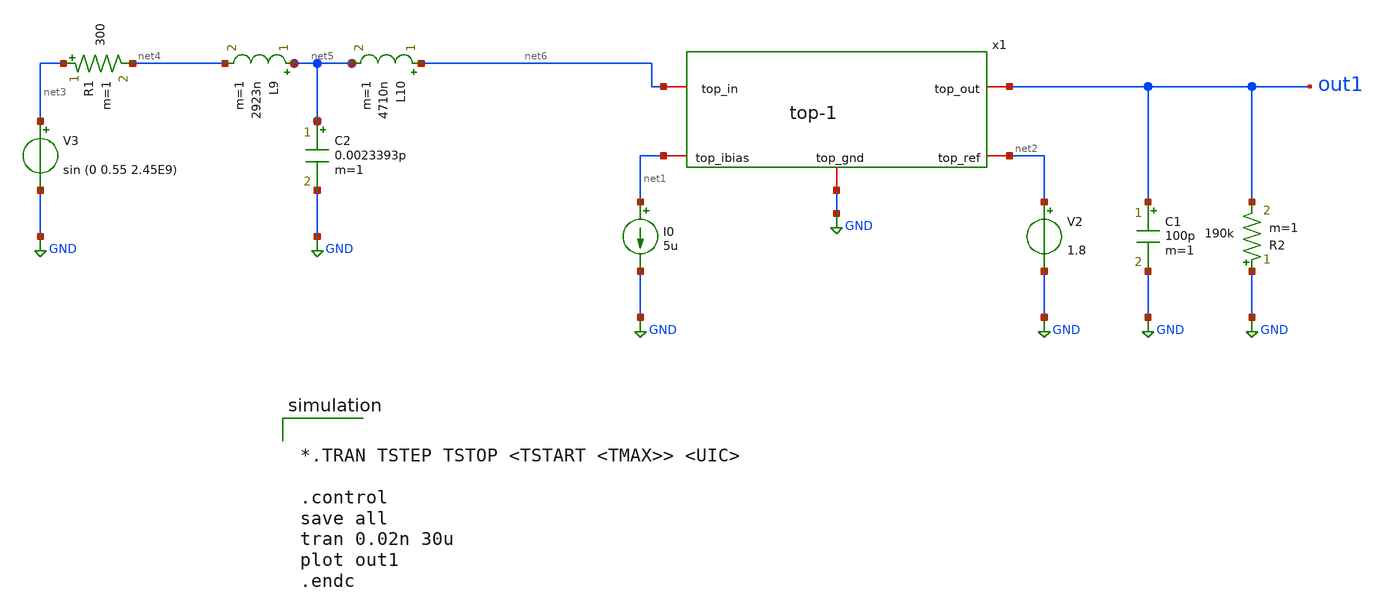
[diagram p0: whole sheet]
** sch_path: xschem/tb-top-1.sch
**.subckt tb-top-1
R2 GND out1 190k m=1
I0 net1 GND 5u
V2 net2 GND 1.8
C1 out1 GND 100p m=1
x1 net6 out1 net2 net1 GND top-1
V3 net3 GND sin (0 0.55 2.45E9)
R1 net3 net4 300 m=1
L9 net5 net4 2923n m=1
C2 net5 GND 0.0023393p m=1
L10 net6 net5 4710n m=1
**** begin user architecture code


*.TRAN TSTEP TSTOP <TSTART <TMAX>> <UIC>

.control
save all
tran 0.02n 30u
plot out1
.endc



** opencircuitdesign pdks install
.lib $::SKYWATER_MODELS/sky130.lib.spice tt


**** end user architecture code
**.ends

* expanding   symbol:  top-1.sym # of pins=5
** sym_path: xschem/top-1.sym
** sch_path: xschem/top-1.sch
.subckt top-1 top_in top_out top_ref top_ibias top_gnd
*.iopin top_in
*.iopin top_gnd
*.iopin top_ibias
*.iopin top_ref
*.iopin top_out
x1 net1 top_in top_gnd cell
x2 net1 top_out top_ibias top_ref top_gnd LDO
.ends


* expanding   symbol:  cell.sym # of pins=3
** sym_path: xschem/cell.sym
** sch_path: xschem/cell.sch
.subckt cell o i ground
*.iopin ground
*.iopin o
*.iopin i
XM10 net1 net1 ground net1 sky130_fd_pr__pfet_01v8_lvt L=0.35 W=40 nf=5 ad='int((5 + 1)/2) * 40 / 5 * 0.29'
+ as='int((5 + 2)/2) * 40 / 5 * 0.29' pd='2*int((5 + 1)/2) * (40 / 5 + 0.29)' ps='2*int((5 + 2)/2) * (40 / 5 + 0.29)'
+ nrd='0.29 / 40 ' nrs='0.29 / 40 ' sa=0 sb=0 sd=0 mult=1 m=1
XM1 o o net1 o sky130_fd_pr__pfet_01v8_lvt L=0.35 W=40 nf=5 ad='int((5 + 1)/2) * 40 / 5 * 0.29' as='int((5 + 2)/2) * 40 / 5 * 0.29'
+ pd='2*int((5 + 1)/2) * (40 / 5 + 0.29)' ps='2*int((5 + 2)/2) * (40 / 5 + 0.29)' nrd='0.29 / 40 ' nrs='0.29 / 40 '
+ sa=0 sb=0 sd=0 mult=1 m=1
XC3 o ground sky130_fd_pr__cap_mim_m3_1 W=30 L=30 MF=3 m=3
XC2 net1 i sky130_fd_pr__cap_mim_m3_1 W=30 L=30 MF=1 m=1
.ends


* expanding   symbol:  LDO.sym # of pins=5
** sym_path: xschem/LDO.sym
** sch_path: xschem/LDO.sch
.subckt LDO ldo_in ldo_out ldo_ibias ldo_ref ldo_gnd
*.iopin ldo_out
*.iopin ldo_in
*.iopin ldo_gnd
*.iopin ldo_ref
*.iopin ldo_ibias
x1 ldo_in ldo_out ldo_ref net1 ldo_ibias ldo_gnd Ota_esq
XM1 ldo_in net1 ldo_out ldo_gnd sky130_fd_pr__nfet_03v3_nvt L=0.5 W=10 nf=1 ad='int((nf+1)/2) * W/nf * 0.29'
+ as='int((nf+2)/2) * W/nf * 0.29' pd='2*int((nf+1)/2) * (W/nf + 0.29)' ps='2*int((nf+2)/2) * (W/nf + 0.29)'
+ nrd='0.29 / W' nrs='0.29 / W' sa=0 sb=0 sd=0 mult=1 m=1
.ends


* expanding   symbol:  Ota_esq.sym # of pins=6
** sym_path: xschem/Ota_esq.sym
** sch_path: xschem/Ota_esq.sch
.subckt Ota_esq VDD Vin Vip Vout Ibias VSS
*.ipin Vin
*.ipin Vip
*.iopin VDD
*.iopin VSS
*.iopin Ibias
*.opin Vout
XC1 net2 Vout sky130_fd_pr__cap_mim_m3_1 W=23 L=23 MF=1 m=1
XM3 VSS net1 net1 VSS sky130_fd_pr__nfet_g5v0d10v5 L=0.5 W=7 nf=1 ad='int((nf+1)/2) * W/nf * 0.29' as='int((nf+2)/2) * W/nf * 0.29'
+ pd='2*int((nf+1)/2) * (W/nf + 0.29)' ps='2*int((nf+2)/2) * (W/nf + 0.29)' nrd='0.29 / W' nrs='0.29 / W'
+ sa=0 sb=0 sd=0 mult=1 m=1
XM1 net1 Vin net3 net3 sky130_fd_pr__pfet_g5v0d10v5 L=0.5 W=2 nf=1 ad='int((nf+1)/2) * W/nf * 0.29' as='int((nf+2)/2) * W/nf * 0.29'
+ pd='2*int((nf+1)/2) * (W/nf + 0.29)' ps='2*int((nf+2)/2) * (W/nf + 0.29)' nrd='0.29 / W' nrs='0.29 / W'
+ sa=0 sb=0 sd=0 mult=1 m=1
XM2 net3 Vip net2 net3 sky130_fd_pr__pfet_g5v0d10v5 L=0.5 W=2 nf=1 ad='int((nf+1)/2) * W/nf * 0.29' as='int((nf+2)/2) * W/nf * 0.29'
+ pd='2*int((nf+1)/2) * (W/nf + 0.29)' ps='2*int((nf+2)/2) * (W/nf + 0.29)' nrd='0.29 / W' nrs='0.29 / W'
+ sa=0 sb=0 sd=0 mult=1 m=1
XM4 net2 net1 VSS VSS sky130_fd_pr__nfet_g5v0d10v5 L=0.5 W=7 nf=1 ad='int((nf+1)/2) * W/nf * 0.29' as='int((nf+2)/2) * W/nf * 0.29'
+ pd='2*int((nf+1)/2) * (W/nf + 0.29)' ps='2*int((nf+2)/2) * (W/nf + 0.29)' nrd='0.29 / W' nrs='0.29 / W'
+ sa=0 sb=0 sd=0 mult=1 m=1
XM7 Vout net2 VSS VSS sky130_fd_pr__nfet_g5v0d10v5 L=1 W=21 nf=7 ad='int((nf+1)/2) * W/nf * 0.29' as='int((nf+2)/2) * W/nf * 0.29'
+ pd='2*int((nf+1)/2) * (W/nf + 0.29)' ps='2*int((nf+2)/2) * (W/nf + 0.29)' nrd='0.29 / W' nrs='0.29 / W'
+ sa=0 sb=0 sd=0 mult=1 m=1
XM8 VDD Ibias Ibias VDD sky130_fd_pr__pfet_g5v0d10v5 L=1 W=24 nf=8 ad='int((nf+1)/2) * W/nf * 0.29' as='int((nf+2)/2) * W/nf * 0.29'
+ pd='2*int((nf+1)/2) * (W/nf + 0.29)' ps='2*int((nf+2)/2) * (W/nf + 0.29)' nrd='0.29 / W' nrs='0.29 / W'
+ sa=0 sb=0 sd=0 mult=1 m=1
XM5 net3 Ibias VDD VDD sky130_fd_pr__pfet_g5v0d10v5 L=1 W=24 nf=8 ad='int((nf+1)/2) * W/nf * 0.29' as='int((nf+2)/2) * W/nf * 0.29'
+ pd='2*int((nf+1)/2) * (W/nf + 0.29)' ps='2*int((nf+2)/2) * (W/nf + 0.29)' nrd='0.29 / W' nrs='0.29 / W'
+ sa=0 sb=0 sd=0 mult=1 m=1
XM6 Vout Ibias VDD VDD sky130_fd_pr__pfet_g5v0d10v5 L=1 W=39 nf=13 ad='int((nf+1)/2) * W/nf * 0.29' as='int((nf+2)/2) * W/nf * 0.29'
+ pd='2*int((nf+1)/2) * (W/nf + 0.29)' ps='2*int((nf+2)/2) * (W/nf + 0.29)' nrd='0.29 / W' nrs='0.29 / W'
+ sa=0 sb=0 sd=0 mult=1 m=1
.ends

.GLOBAL GND
.end
